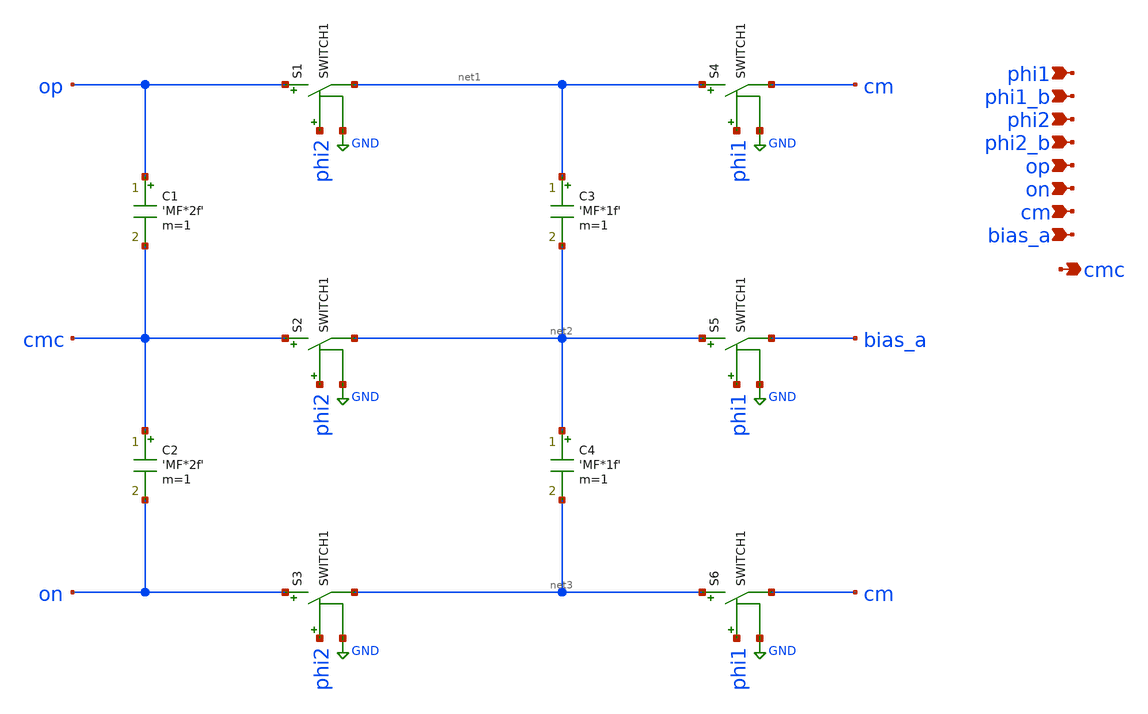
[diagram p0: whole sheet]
** sch_path: design/analog_modulator/schematic/ideal_sc_cmfb.sch
**.subckt ideal_sc_cmfb on cm bias_a op cmc phi2_b phi2 phi1_b phi1
*.ipin on
*.ipin cm
*.ipin bias_a
*.ipin op
*.opin cmc
*.ipin phi2_b
*.ipin phi2
*.ipin phi1_b
*.ipin phi1
C1 op cmc 'MF*2f' m=1
C2 cmc on 'MF*2f' m=1
C3 net1 net2 'MF*1f' m=1
C4 net2 net3 'MF*1f' m=1
S1 op net1 phi2 GND SWITCH1
S2 cmc net2 phi2 GND SWITCH1
S3 on net3 phi2 GND SWITCH1
S4 net1 cm phi1 GND SWITCH1
S5 net2 bias_a phi1 GND SWITCH1
S6 net3 cm phi1 GND SWITCH1
**.ends
.GLOBAL GND
.end
